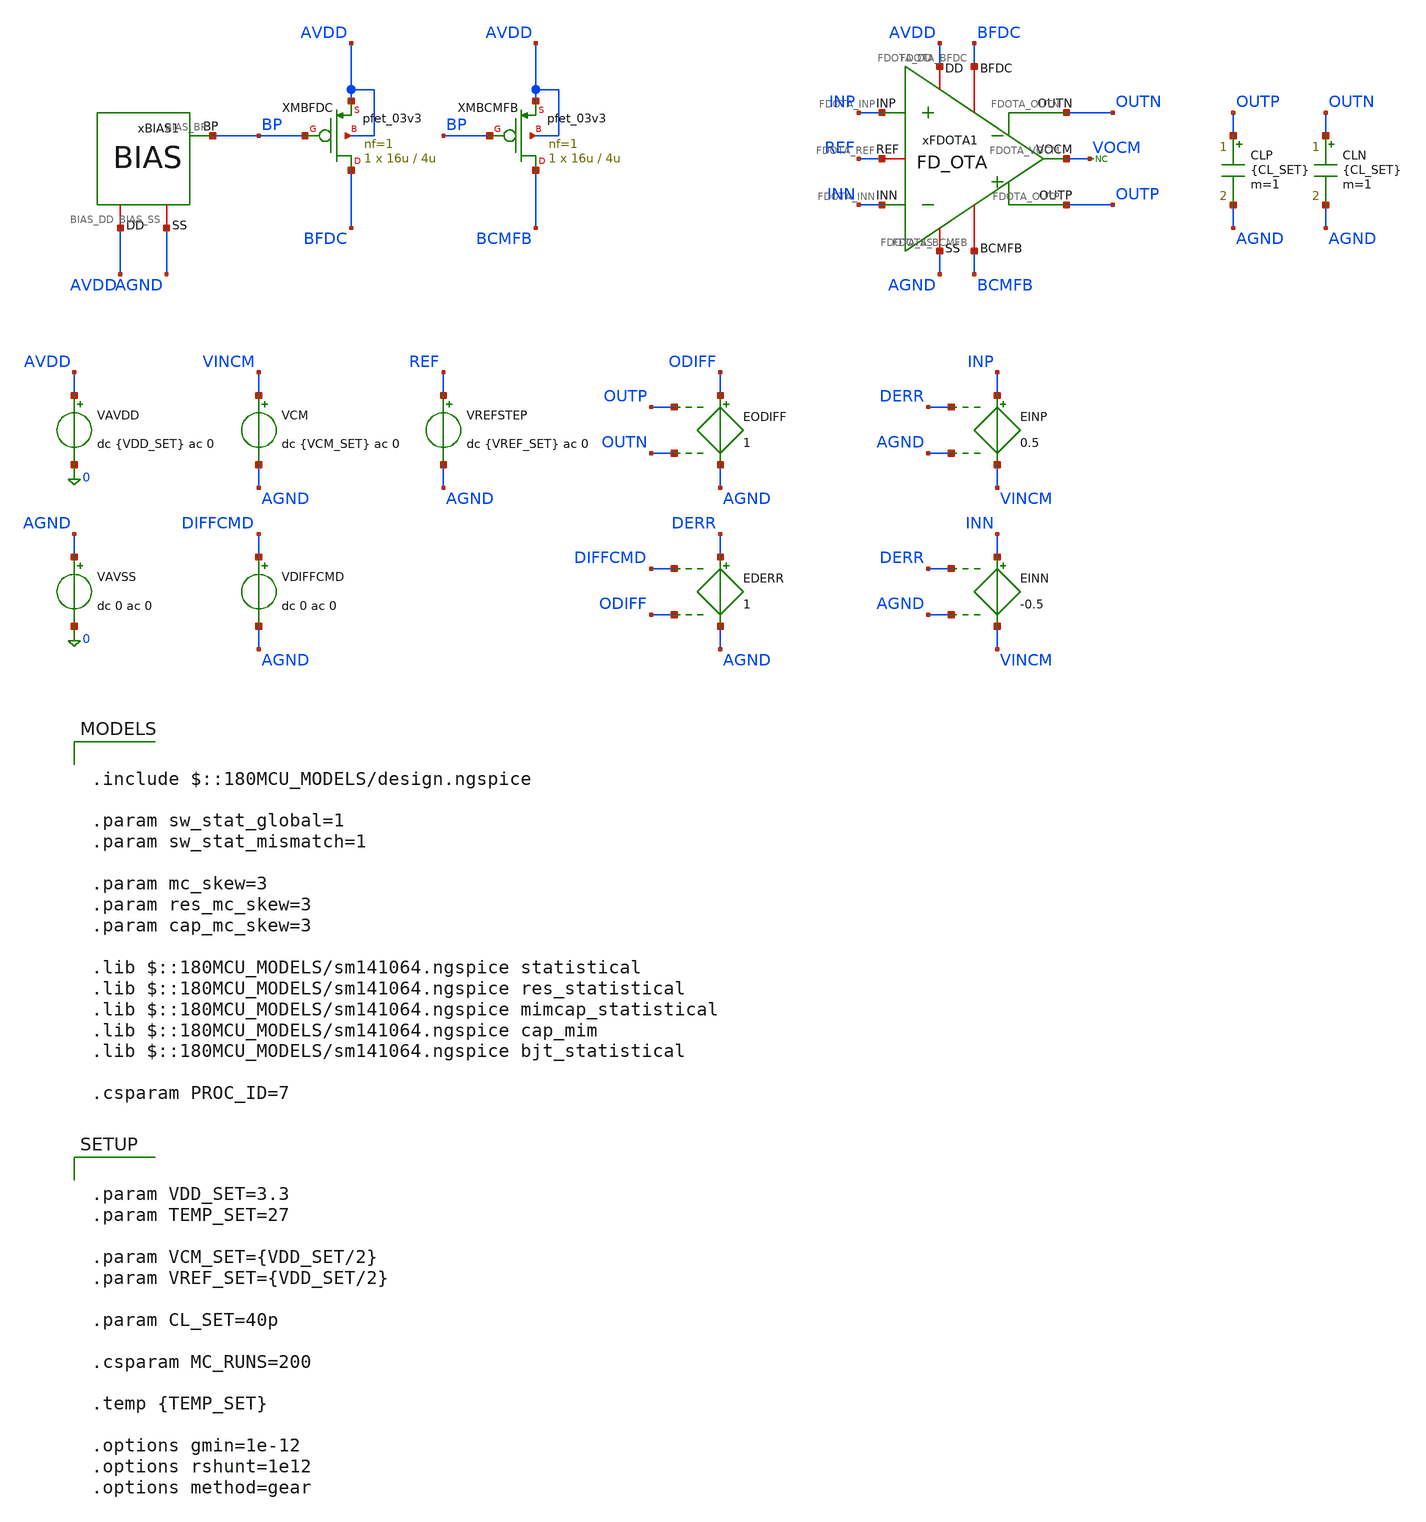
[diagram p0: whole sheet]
** sch_path: Design_Files/IC Design/Testbench/ANALOG_BLOCKS/FD_OTA/Close_Loop/FD_OTA_TB_CL_FULL.sch
**.subckt FD_OTA_TB_CL_FULL
VAVDD AVDD 0 dc {VDD_SET} ac 0
.save i(vavdd)
VCM VINCM AGND dc {VCM_SET} ac 0
VAVSS AGND 0 dc 0 ac 0
VDIFFCMD DIFFCMD AGND dc 0 ac 0
CLP OUTP AGND {CL_SET} m=1
CLN OUTN AGND {CL_SET} m=1
* noconn VOCM
EODIFF ODIFF AGND OUTP OUTN 1
EDERR DERR AGND DIFFCMD ODIFF 1
xFDOTA1 AVDD AGND INP INN OUTN BFDC OUTP BCMFB REF VOCM FD_OTA
xBIAS1 AVDD AGND BP BIAS
XMBFDC BFDC BP AVDD AVDD pfet_03v3 L=4u W=16u nf=1 ad='int((nf+1)/2) * W/nf * 0.18u' as='int((nf+2)/2) * W/nf * 0.18u'
+ pd='2*int((nf+1)/2) * (W/nf + 0.18u)' ps='2*int((nf+2)/2) * (W/nf + 0.18u)' nrd='0.18u / W' nrs='0.18u / W'
+ sa=0 sb=0 sd=0 m=1
XMBCMFB BCMFB BP AVDD AVDD pfet_03v3 L=4u W=16u nf=1 ad='int((nf+1)/2) * W/nf * 0.18u' as='int((nf+2)/2) * W/nf * 0.18u'
+ pd='2*int((nf+1)/2) * (W/nf + 0.18u)' ps='2*int((nf+2)/2) * (W/nf + 0.18u)' nrd='0.18u / W' nrs='0.18u / W'
+ sa=0 sb=0 sd=0 m=1
EINP INP VINCM DERR AGND 0.5
EINN INN VINCM DERR AGND -0.5
VREFSTEP REF AGND dc {VREF_SET} ac 0
**** begin user architecture code

.include $::180MCU_MODELS/design.ngspice

.param sw_stat_global=1
.param sw_stat_mismatch=1

.param mc_skew=3
.param res_mc_skew=3
.param cap_mc_skew=3

.lib $::180MCU_MODELS/sm141064.ngspice statistical
.lib $::180MCU_MODELS/sm141064.ngspice res_statistical
.lib $::180MCU_MODELS/sm141064.ngspice mimcap_statistical
.lib $::180MCU_MODELS/sm141064.ngspice cap_mim
.lib $::180MCU_MODELS/sm141064.ngspice bjt_statistical

.csparam PROC_ID=7




.control

destroy all

set noaskquit
set wr_singlescale
unset wr_vecnames

option klu
option numdgt=15
option method=gear
option maxord=2
option plotwinsize=0
option rshunt=1e12


if $&PROC_ID = 5
set proc=MM
else
if $&PROC_ID = 6
set proc=GL
else
set proc=FULL
end
end


shell mkdir -p /foss/designs/ECG_Acquisition_IC/Measurement_Results/IC_Simulation/ANALOG_BLOCKS/FD_OTA/{$proc}.Result_txt

shell rm -f /foss/designs/ECG_Acquisition_IC/Measurement_Results/IC_Simulation/ANALOG_BLOCKS/FD_OTA/{$proc}.Result_txt/{$proc}.cl_mc_summary.txt
shell rm -f /foss/designs/ECG_Acquisition_IC/Measurement_Results/IC_Simulation/ANALOG_BLOCKS/FD_OTA/{$proc}.Result_txt/{$proc}.cl_mc_debug_op.txt


echo run out_cm_error_V cl_gain_10 gain_error_pct ibias_fdc_A ibias_cmfb_A idd_A power_W > /foss/designs/ECG_Acquisition_IC/Measurement_Results/IC_Simulation/ANALOG_BLOCKS/FD_OTA/{$proc}.Result_txt/{$proc}.cl_mc_summary.txt

echo run vin_diff_V vos_cl_V outp_V outn_V outcm_V outdiff_V ref_V vocm_V bfdc_V bcmfb_V ibias_fdc_A
+ ibias_cmfb_A idd_A power_W > /foss/designs/ECG_Acquisition_IC/Measurement_Results/IC_Simulation/ANALOG_BLOCKS/FD_OTA/{$proc}.Result_txt/{$proc}.cl_mc_debug_op.txt


let run=1
let mc_runs=$&MC_RUNS


dowhile run <= mc_runs

set runnum=$&run

setseed $runnum
mc_source


option klu
option numdgt=15
option method=gear
option maxord=2
option plotwinsize=0
option rshunt=1e12


* SOURCES

alter @VAVDD[DC]=3.3
alter @VAVSS[DC]=0

alter @VCM[DC]=1.65
alter @VDIFFCMD[DC]=0
alter @VREFSTEP[DC]=1.65

alter @VAVDD[ACMAG]=0
alter @VAVSS[ACMAG]=0
alter @VCM[ACMAG]=0
alter @VDIFFCMD[ACMAG]=0
alter @VREFSTEP[ACMAG]=0


* OP

save AVDD AGND INP INN OUTP OUTN REF VOCM BFDC BCMFB
save vavdd#branch
save @m.xmbfdc.m0[id]
save @m.xmbcmfb.m0[id]

op


let vin_diff=v(INP)-v(INN)

let outp=v(OUTP)-v(AGND)
let outn=v(OUTN)-v(AGND)

let outcm=0.5*(outp+outn)
let outdiff=outp-outn

let ref=v(REF)-v(AGND)
let vocm=v(VOCM)-v(AGND)

let out_cm_error=outcm-ref

let vos_cl=-vin_diff

let bfdc=v(BFDC)-v(AGND)
let bcmfb=v(BCMFB)-v(AGND)

let ibias_fdc=abs(@m.xmbfdc.m0[id])
let ibias_cmfb=abs(@m.xmbcmfb.m0[id])

let idd_total=abs(vavdd#branch)
let power_total=(v(AVDD)-v(AGND))*idd_total


set vin_diff_val=$&vin_diff
set vos_cl_val=$&vos_cl

set outp_val=$&outp
set outn_val=$&outn
set outcm_val=$&outcm
set outdiff_val=$&outdiff

set ref_val=$&ref
set vocm_val=$&vocm

set out_cm_error_val=$&out_cm_error

set bfdc_val=$&bfdc
set bcmfb_val=$&bcmfb

set ibias_fdc_val=$&ibias_fdc
set ibias_cmfb_val=$&ibias_cmfb

set idd_val=$&idd_total
set power_val=$&power_total


echo $runnum $vin_diff_val $vos_cl_val $outp_val $outn_val $outcm_val $outdiff_val $ref_val $vocm_val
+ $bfdc_val $bcmfb_val $ibias_fdc_val $ibias_cmfb_val $idd_val $power_val >> /foss/designs/ECG_Acquisition_IC/Measurement_Results/IC_Simulation/ANALOG_BLOCKS/FD_OTA/{$proc}.Result_txt/{$proc}.cl_mc_debug_op.txt


destroy all


* DIFF AC

alter @VAVDD[ACMAG]=0
alter @VAVSS[ACMAG]=0
alter @VCM[ACMAG]=0
alter @VREFSTEP[ACMAG]=0

alter @VDIFFCMD[DC]=0
alter @VDIFFCMD[ACMAG]=1
alter @VDIFFCMD[ACPHASE]=0

save AGND OUTP OUTN DIFFCMD

ac dec 100 0.1 100Meg


let cmd_ac=v(DIFFCMD)-v(AGND)
let outdiff_ac=v(OUTP)-v(OUTN)

let cl_tf=outdiff_ac/cmd_ac
let cl_gain=mag(cl_tf)

meas ac cl_gain_10_meas find cl_gain at=10

let gain_error_pct=100*(cl_gain_10_meas-1)

set cl_gain_val=$&cl_gain_10_meas
set gain_error_val=$&gain_error_pct


echo $runnum $out_cm_error_val $cl_gain_val $gain_error_val $ibias_fdc_val $ibias_cmfb_val $idd_val $power_val
+ >> /foss/designs/ECG_Acquisition_IC/Measurement_Results/IC_Simulation/ANALOG_BLOCKS/FD_OTA/{$proc}.Result_txt/{$proc}.cl_mc_summary.txt


destroy all

let run=run+1

end


quit

.endc




.param VDD_SET=3.3
.param TEMP_SET=27

.param VCM_SET={VDD_SET/2}
.param VREF_SET={VDD_SET/2}

.param CL_SET=40p

.csparam MC_RUNS=200

.temp {TEMP_SET}

.options gmin=1e-12
.options rshunt=1e12
.options method=gear


**** end user architecture code
**.ends
.end
